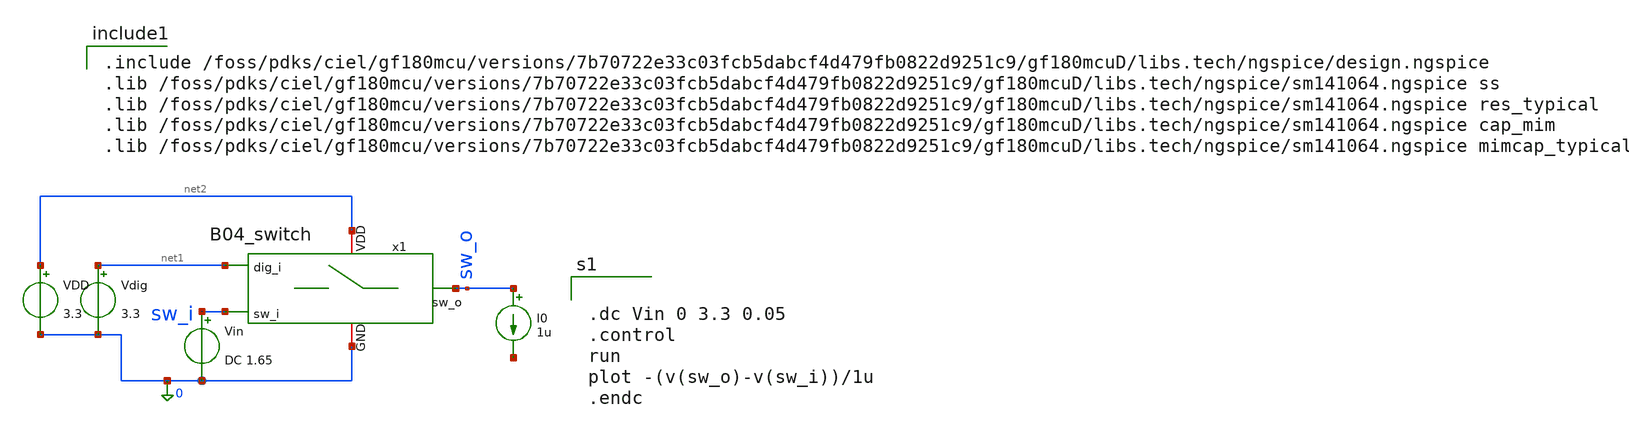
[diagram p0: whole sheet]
** sch_path: analog/B04_tb_switch.sch
**.subckt B04_tb_switch
x1 net2 net1 sw_i sw_o 0 B04_switch
Vdig net1 0 3.3
Vin sw_i 0 DC 1.65
VDD net2 0 3.3
I0 sw_o net3 1u
**** begin user architecture code


.dc Vin 0 3.3 0.05
.control
run
plot -(v(sw_o)-v(sw_i))/1u
.endc



.include /foss/pdks/ciel/gf180mcu/versions/7b70722e33c03fcb5dabcf4d479fb0822d9251c9/gf180mcuD/libs.tech/ngspice/design.ngspice
.lib /foss/pdks/ciel/gf180mcu/versions/7b70722e33c03fcb5dabcf4d479fb0822d9251c9/gf180mcuD/libs.tech/ngspice/sm141064.ngspice ss
.lib /foss/pdks/ciel/gf180mcu/versions/7b70722e33c03fcb5dabcf4d479fb0822d9251c9/gf180mcuD/libs.tech/ngspice/sm141064.ngspice res_typical
.lib /foss/pdks/ciel/gf180mcu/versions/7b70722e33c03fcb5dabcf4d479fb0822d9251c9/gf180mcuD/libs.tech/ngspice/sm141064.ngspice cap_mim
.lib /foss/pdks/ciel/gf180mcu/versions/7b70722e33c03fcb5dabcf4d479fb0822d9251c9/gf180mcuD/libs.tech/ngspice/sm141064.ngspice mimcap_typical

**** end user architecture code
**.ends

* expanding   symbol:
*+  AURA-Event-Driven-Mixed-Signal-ASIC-for-Acoustic-Pattern-Detection/analog/B04_switch.sym # of pins=5
** sym_path: analog/B04_switch.sym
** sch_path: analog/B04_switch.sch
.subckt B04_switch VDD dig_i sw_i sw_o GND
*.iopin VDD
*.iopin GND
*.ipin sw_i
*.opin sw_o
*.ipin dig_i
XM1 sw_o net1 sw_i VDD pfet_03v3 L=0.28u W=0.88u nf=1 ad='int((nf+1)/2) * W/nf * 0.18u' as='int((nf+2)/2) * W/nf * 0.18u'
+ pd='2*int((nf+1)/2) * (W/nf + 0.18u)' ps='2*int((nf+2)/2) * (W/nf + 0.18u)' nrd='0.18u / W' nrs='0.18u / W'
+ sa=0 sb=0 sd=0 m=1
XM2 sw_i dig_i sw_o GND nfet_03v3 L=0.28u W=0.22u nf=1 ad='int((nf+1)/2) * W/nf * 0.18u' as='int((nf+2)/2) * W/nf * 0.18u'
+ pd='2*int((nf+1)/2) * (W/nf + 0.18u)' ps='2*int((nf+2)/2) * (W/nf + 0.18u)' nrd='0.18u / W' nrs='0.18u / W'
+ sa=0 sb=0 sd=0 m=1
XM3 net1 dig_i VDD VDD pfet_03v3 L=0.28u W=0.22u nf=1 ad='int((nf+1)/2) * W/nf * 0.18u' as='int((nf+2)/2) * W/nf * 0.18u'
+ pd='2*int((nf+1)/2) * (W/nf + 0.18u)' ps='2*int((nf+2)/2) * (W/nf + 0.18u)' nrd='0.18u / W' nrs='0.18u / W'
+ sa=0 sb=0 sd=0 m=1
XM4 net1 dig_i GND GND nfet_03v3 L=0.28u W=0.22u nf=1 ad='int((nf+1)/2) * W/nf * 0.18u' as='int((nf+2)/2) * W/nf * 0.18u'
+ pd='2*int((nf+1)/2) * (W/nf + 0.18u)' ps='2*int((nf+2)/2) * (W/nf + 0.18u)' nrd='0.18u / W' nrs='0.18u / W'
+ sa=0 sb=0 sd=0 m=1
.ends

.end
